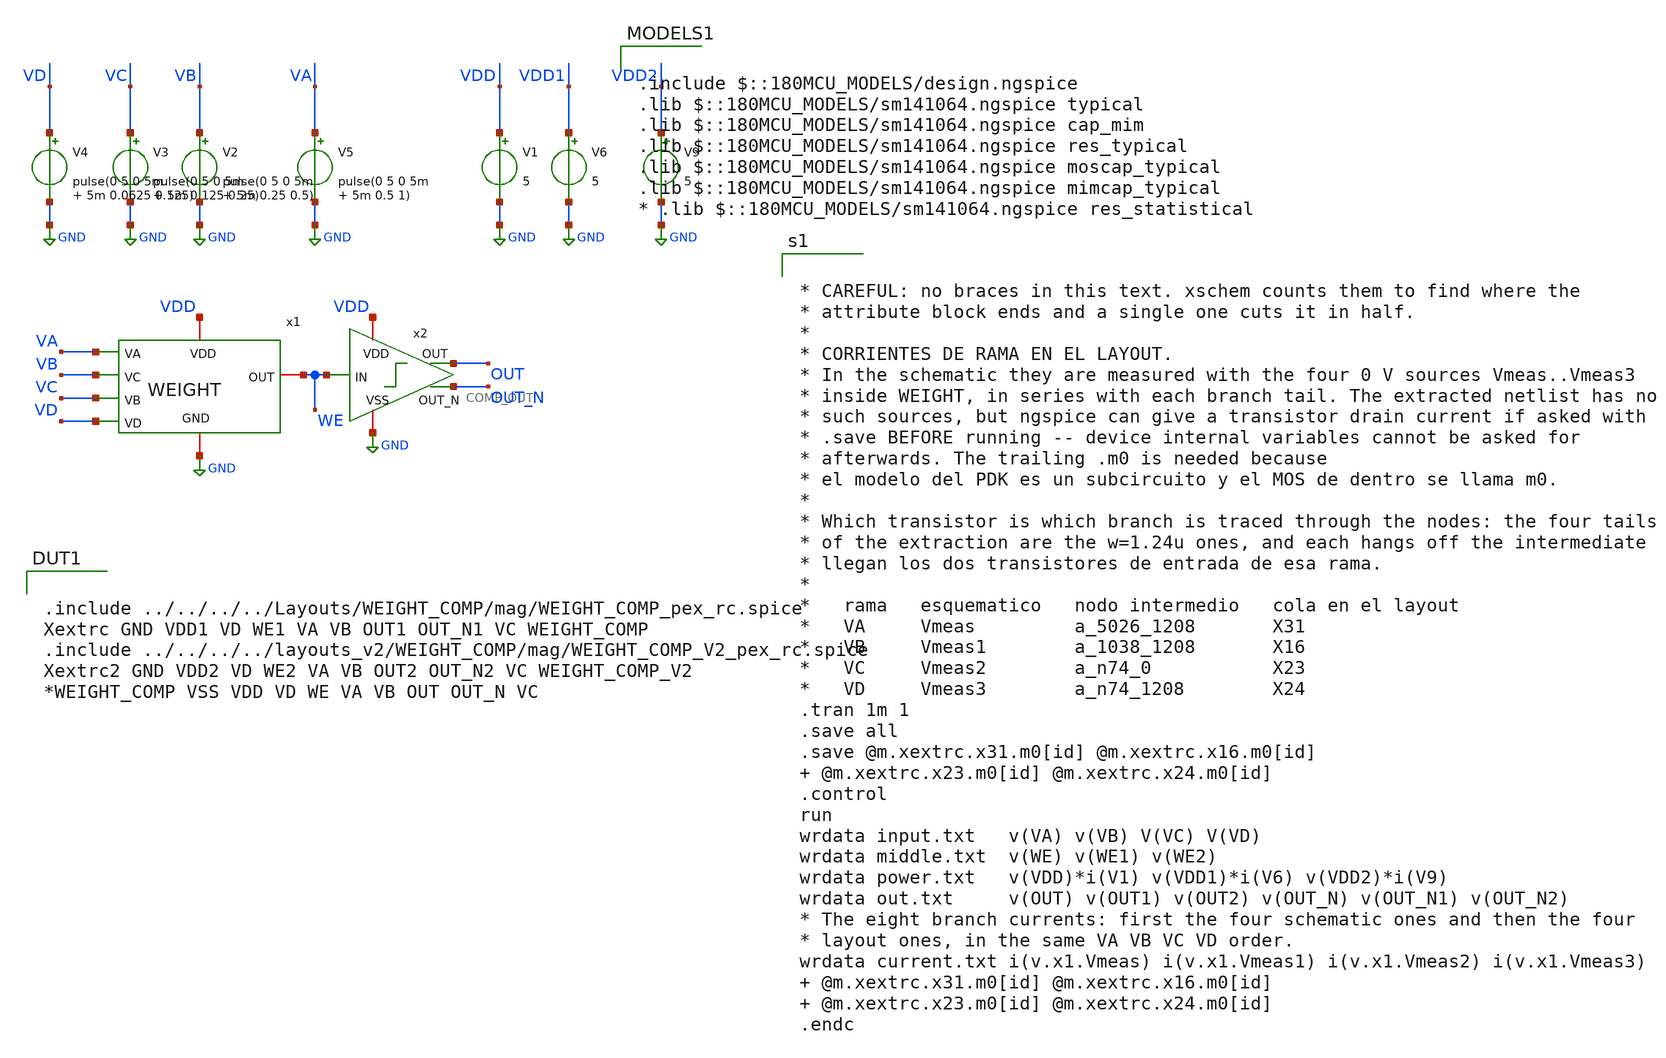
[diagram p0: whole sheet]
** sch_path: FINAL/XSCHEM/TEST/test_weight.sch
**.subckt test_weight
V1 VDD GND 5
V5 VA GND pulse(0 5 0 5m 5m 0.5 1)
x1 VDD GND WE VA VB VC VD WEIGHT
x2 VDD OUT WE OUT_N GND COMP_OUT
V6 VDD1 GND 5
V9 VDD2 GND 5
V2 VB GND pulse(0 5 0 5m 5m 0.25 0.5)
V3 VC GND pulse(0 5 0 5m 5m 0.125 0.25)
V4 VD GND pulse(0 5 0 5m 5m 0.0625 0.125)
**** begin user architecture code


* CAREFUL: no braces in this text. xschem counts them to find where the
* attribute block ends and a single one cuts it in half.
*
* CORRIENTES DE RAMA EN EL LAYOUT.
* In the schematic they are measured with the four 0 V sources Vmeas..Vmeas3
* inside WEIGHT, in series with each branch tail. The extracted netlist has no
* such sources, but ngspice can give a transistor drain current if asked with
* .save BEFORE running -- device internal variables cannot be asked for
* afterwards. The trailing .m0 is needed because
* el modelo del PDK es un subcircuito y el MOS de dentro se llama m0.
*
* Which transistor is which branch is traced through the nodes: the four tails
* of the extraction are the w=1.24u ones, and each hangs off the intermediate
* llegan los dos transistores de entrada de esa rama.
*
*   rama   esquematico   nodo intermedio   cola en el layout
*   VA     Vmeas         a_5026_1208       X31
*   VB     Vmeas1        a_1038_1208       X16
*   VC     Vmeas2        a_n74_0           X23
*   VD     Vmeas3        a_n74_1208        X24
.tran 1m 1
.save all
.save @m.xextrc.x31.m0[id] @m.xextrc.x16.m0[id]  @m.xextrc.x23.m0[id] @m.xextrc.x24.m0[id]
.control
run
wrdata input.txt   v(VA) v(VB) V(VC) V(VD)
wrdata middle.txt  v(WE) v(WE1) v(WE2)
wrdata power.txt   v(VDD)*i(V1) v(VDD1)*i(V6) v(VDD2)*i(V9)
wrdata out.txt     v(OUT) v(OUT1) v(OUT2) v(OUT_N) v(OUT_N1) v(OUT_N2)
* The eight branch currents: first the four schematic ones and then the four
* layout ones, in the same VA VB VC VD order.
wrdata current.txt i(v.x1.Vmeas) i(v.x1.Vmeas1) i(v.x1.Vmeas2) i(v.x1.Vmeas3)  @m.xextrc.x31.m0[id]
+ @m.xextrc.x16.m0[id]  @m.xextrc.x23.m0[id] @m.xextrc.x24.m0[id]
.endc



.include $::180MCU_MODELS/design.ngspice
.lib $::180MCU_MODELS/sm141064.ngspice typical
.lib $::180MCU_MODELS/sm141064.ngspice cap_mim
.lib $::180MCU_MODELS/sm141064.ngspice res_typical
.lib $::180MCU_MODELS/sm141064.ngspice moscap_typical
.lib $::180MCU_MODELS/sm141064.ngspice mimcap_typical
* .lib $::180MCU_MODELS/sm141064.ngspice res_statistical


.include ../../../../Layouts/WEIGHT_COMP/mag/WEIGHT_COMP_pex_rc.spice
Xextrc GND VDD1 VD WE1 VA VB OUT1 OUT_N1 VC WEIGHT_COMP
.include ../../../../layouts_v2/WEIGHT_COMP/mag/WEIGHT_COMP_V2_pex_rc.spice
Xextrc2 GND VDD2 VD WE2 VA VB OUT2 OUT_N2 VC WEIGHT_COMP_V2
*WEIGHT_COMP VSS VDD VD WE VA VB OUT OUT_N VC

**** end user architecture code
**.ends
.GLOBAL GND
.end
